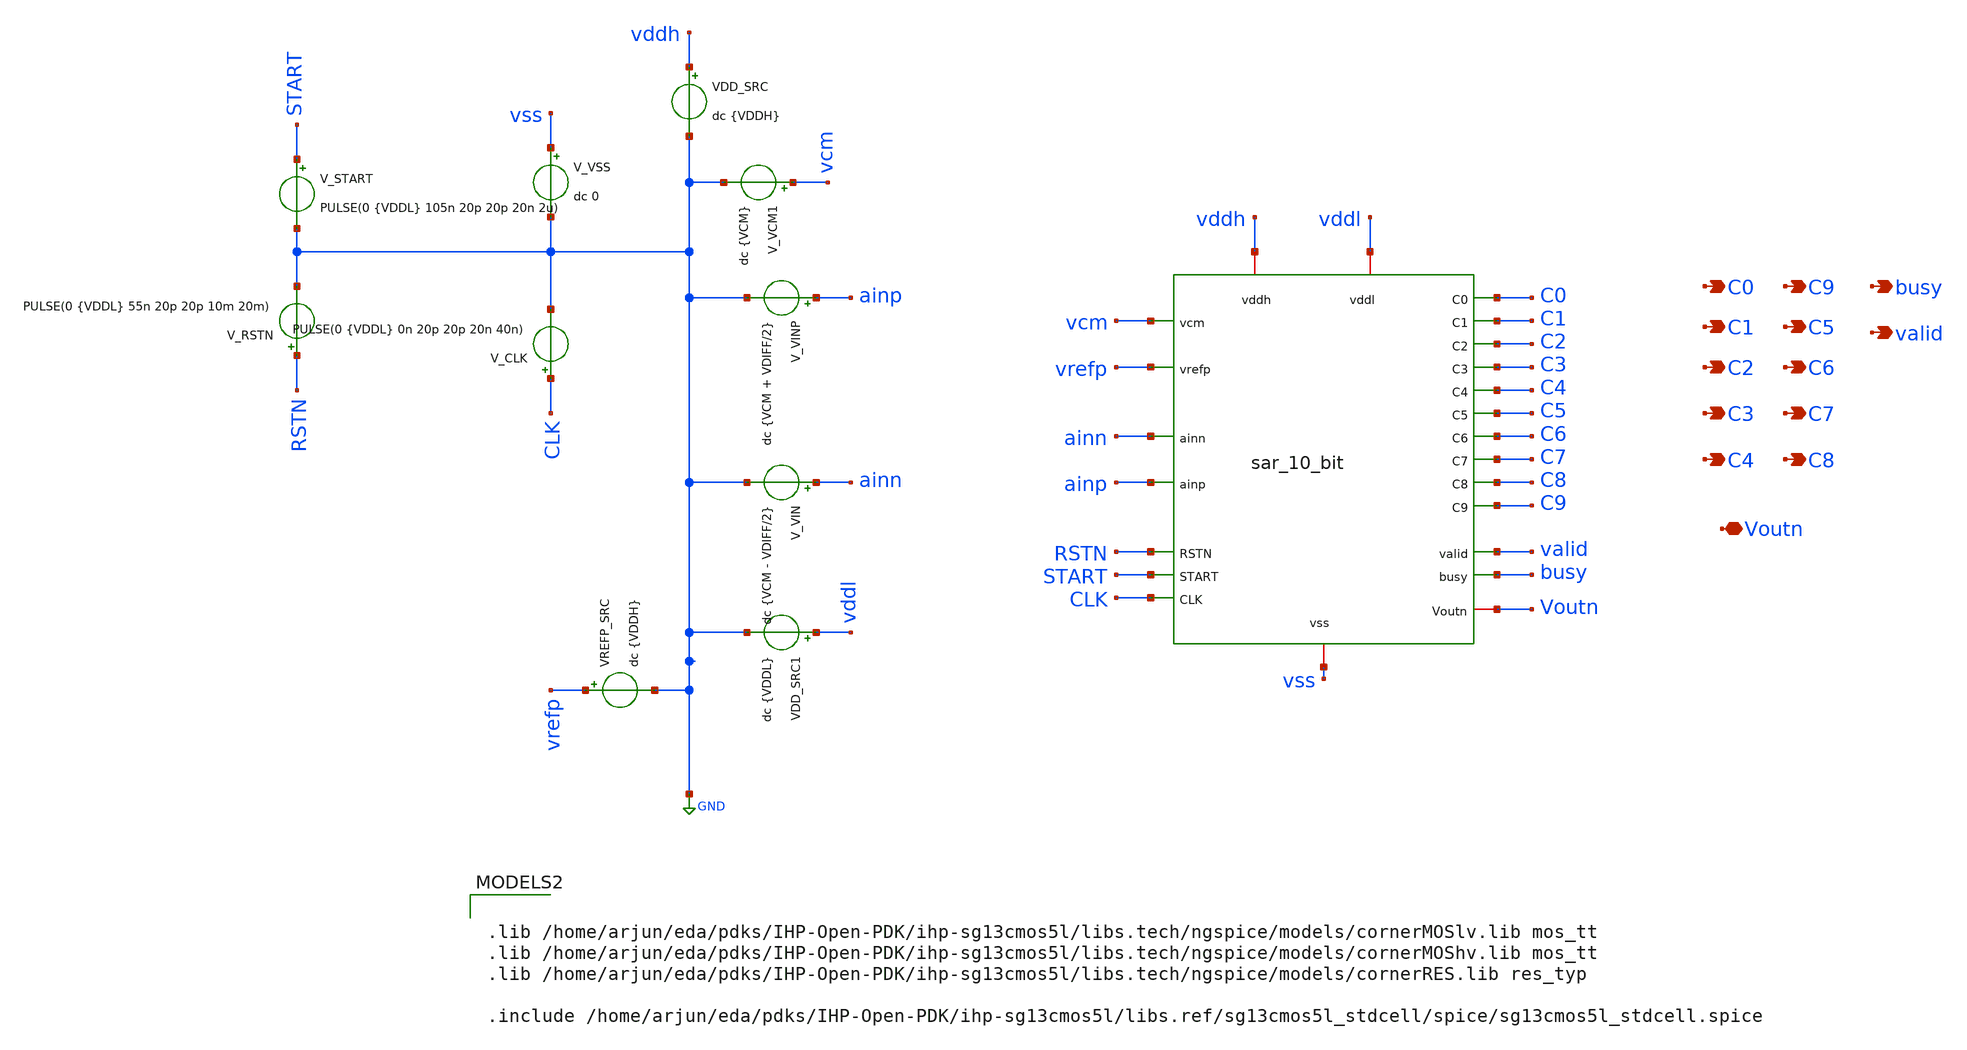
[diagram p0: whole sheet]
** sch_path: circuit_files/sar_adc_test/tb/sar_10_bit_tb_1.sch
**.subckt sar_10_bit_tb_1 C1 C2 C3 C4 C5 C6 C7 C8 C0 C9 busy valid Voutn
*.opin C1
*.opin C2
*.opin C3
*.opin C4
*.opin C5
*.opin C6
*.opin C7
*.opin C8
*.opin C0
*.opin C9
*.opin busy
*.opin valid
*.iopin Voutn
x1 RSTN busy START valid vcm vrefp ainn ainp CLK C0 C9 C1 C5 C6 C2 C7 C3 C8 C4 vss vddh Voutn vddl
+ sar_10_bit
V_VIN ainn GND dc {VCM - VDIFF/2}
VDD_SRC vddh GND dc {VDDH}
V_VINP ainp GND dc {VCM + VDIFF/2}
V_VSS vss GND dc 0
V_CLK CLK GND PULSE(0 {VDDL} 0n 20p 20p 20n 40n)
V_VCM1 vcm GND dc {VCM}
VREFP_SRC vrefp GND dc {VDDH}
V_RSTN RSTN GND PULSE(0 {VDDL} 55n 20p 20p 10m 20m)
V_START START GND PULSE(0 {VDDL} 105n 20p 20p 20n 2u)
VDD_SRC1 vddl GND dc {VDDL}
**** begin user architecture code

.lib /home/arjun/eda/pdks/IHP-Open-PDK/ihp-sg13cmos5l/libs.tech/ngspice/models/cornerMOSlv.lib mos_tt
.lib /home/arjun/eda/pdks/IHP-Open-PDK/ihp-sg13cmos5l/libs.tech/ngspice/models/cornerMOShv.lib mos_tt
.lib /home/arjun/eda/pdks/IHP-Open-PDK/ihp-sg13cmos5l/libs.tech/ngspice/models/cornerRES.lib res_typ

.include /home/arjun/eda/pdks/IHP-Open-PDK/ihp-sg13cmos5l/libs.ref/sg13cmos5l_stdcell/spice/sg13cmos5l_stdcell.spice





.param VDDH=3.3
.param VDDL=1.2

.param VREF=3.3
.param VCM=1.65

.param NBITS=10
.param Cu=10f

* LSB = 3.3 / 1024 = 3.22265625 mV
.param VDIFF=0


*.options savecurrents
.options reltol=1e-4
.options abstol=1e-12
.options vntol=1e-6

.options method=gear
.options maxord=2

.options plotwinsize=0
.options itl4=500

.save v(ainp)
.save v(ainn)
.save v(x1.vcp)
.save v(x1.vcn)
.save v(x1.sample_hv)
.save v(x1.sampleb_hv)
.save v(x1.comp_clk_hv)
.save v(valid)






.control

set noaskquit
set num_threads=6
set wr_singlescale
set wr_vecnames
option numdgt=12

setplot const

let input_vec = vector(5)
let input_vec[0] = -1.6
let input_vec[1] = -0.8
let input_vec[2] = 0
let input_vec[3] = 0.8
let input_vec[4] = 1.6

let track_vec = 0*vector(5)
let held_vec = 0*vector(5)
let precomp_vec = 0*vector(5)
let cm_vec = 0*vector(5)
let index = 0

echo ============================================================
echo SAR_ADC_SAMPLING_PATH_TEST
echo ============================================================

repeat 5

let vdiff_now = input_vec[index]
let vinp_now = 1.65 + vdiff_now/2
let vinn_now = 1.65 - vdiff_now/2

alter V_VINP $&vinp_now
alter V_VIN $&vinn_now

echo ------------------------------------------------------------
echo TEST_POINT
print index
echo APPLIED_VDIFF
print vdiff_now
echo VINP
print vinp_now
echo VINN
print vinn_now

tran 200p 800n 0 200p

meas tran tsamp_end WHEN v(x1.sample_hv)=1.65 FALL=1 TD=100n
meas tran tcomp_start WHEN v(x1.comp_clk_hv)=1.65 RISE=1 TD=100n

let t_track = tsamp_end - 1n
let t_hold = tsamp_end + 1n
let t_precomp = tcomp_start - 1n
let hold_gap = tcomp_start - tsamp_end

meas tran vcp_track FIND v(x1.vcp) AT=$&t_track
meas tran vcn_track FIND v(x1.vcn) AT=$&t_track
meas tran vcp_hold FIND v(x1.vcp) AT=$&t_hold
meas tran vcn_hold FIND v(x1.vcn) AT=$&t_hold
meas tran vcp_precomp FIND v(x1.vcp) AT=$&t_precomp
meas tran vcn_precomp FIND v(x1.vcn) AT=$&t_precomp

let track_diff = vcp_track - vcn_track
let held_diff = vcp_hold - vcn_hold
let precomp_diff = vcp_precomp - vcn_precomp
let held_cm = (vcp_hold + vcn_hold)/2

let track_vec[index] = track_diff
let held_vec[index] = held_diff
let precomp_vec[index] = precomp_diff
let cm_vec[index] = held_cm

echo SAMPLE_END_TIME
print tsamp_end

echo COMPARATOR_START_TIME
print tcomp_start

echo SAMPLE_TO_COMPARATOR_GAP
print hold_gap

echo DIFFERENTIAL_BEFORE_SAMPLE_OPENS
print track_diff

echo DIFFERENTIAL_AFTER_SAMPLE_OPENS
print held_diff

echo DIFFERENTIAL_BEFORE_COMPARATOR
print precomp_diff

echo HELD_VCP
print vcp_hold

echo HELD_VCN
print vcn_hold

echo HELD_COMMON_MODE
print held_cm

destroy $curplot
setplot const

let index = index + 1

end

setplot const

setscale track_vec input_vec
setscale held_vec input_vec
setscale precomp_vec input_vec
setscale cm_vec input_vec

wrdata sampling_path_test.dat track_vec held_vec precomp_vec cm_vec

echo ============================================================
echo SAMPLING_PATH_TEST_COMPLETE
echo DATA_WRITTEN_TO_sampling_path_test.dat
echo ============================================================

rusage

.endc



**** end user architecture code
**.ends
.GLOBAL GND
.end
